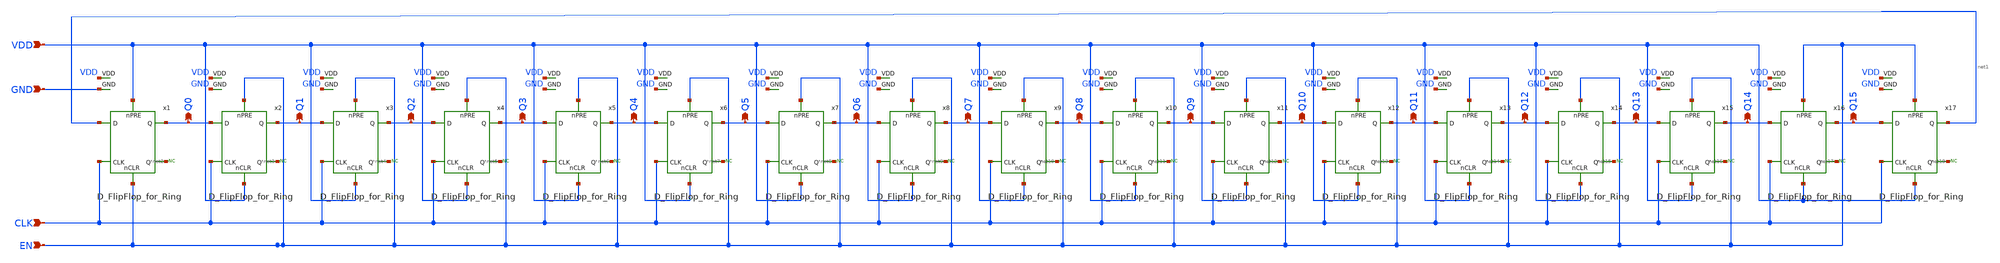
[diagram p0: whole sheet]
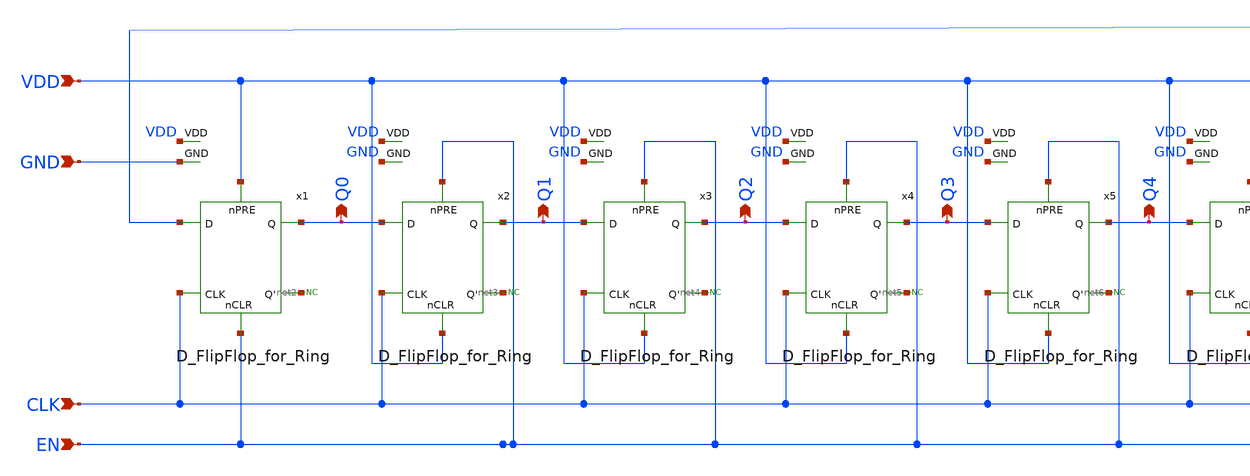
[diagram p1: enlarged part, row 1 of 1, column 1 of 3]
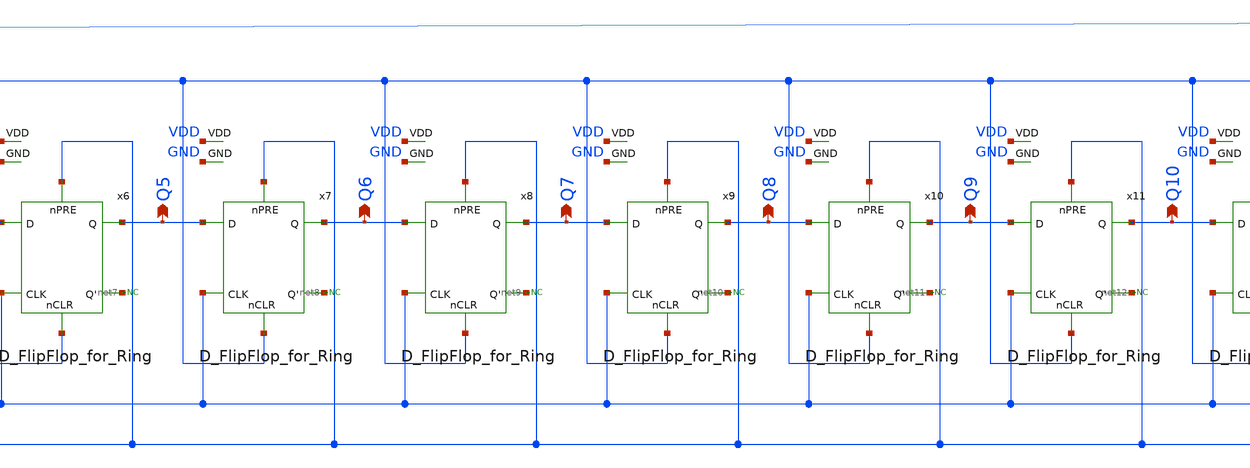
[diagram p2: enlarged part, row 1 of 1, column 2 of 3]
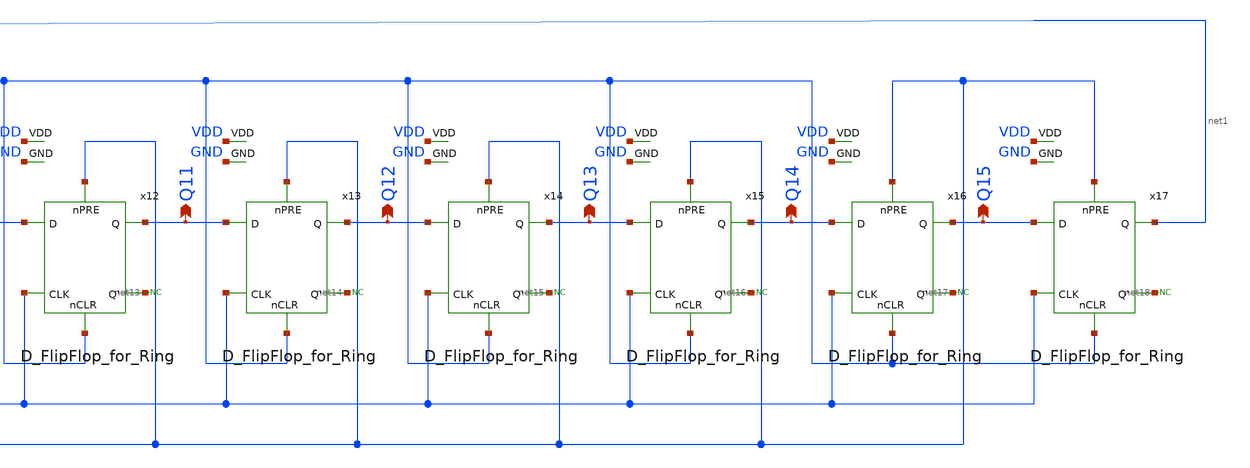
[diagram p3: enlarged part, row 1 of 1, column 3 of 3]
** sch_path: xschem/RING_COUNTER_FINAL.sch
**.subckt RING_COUNTER_FINAL Q0 Q1 Q2 Q3 Q4 Q5 Q6 Q7 Q8 Q9 Q10 Q11 Q12 Q13 Q14 Q15 CLK EN VDD GND
*.opin Q0
*.opin Q1
*.opin Q2
*.opin Q3
*.opin Q4
*.opin Q5
*.opin Q6
*.opin Q7
*.opin Q8
*.opin Q9
*.opin Q10
*.opin Q11
*.opin Q12
*.opin Q13
*.opin Q14
*.opin Q15
*.ipin CLK
*.ipin EN
*.ipin VDD
*.ipin GND
x1 VDD net1 Q0 CLK net2 EN GND VDD D_FlipFlop_for_Ring
x2 EN Q0 Q1 CLK net3 VDD GND VDD D_FlipFlop_for_Ring
x3 EN Q1 Q2 CLK net4 VDD GND VDD D_FlipFlop_for_Ring
x4 EN Q2 Q3 CLK net5 VDD GND VDD D_FlipFlop_for_Ring
x5 EN Q3 Q4 CLK net6 VDD GND VDD D_FlipFlop_for_Ring
x6 EN Q4 Q5 CLK net7 VDD GND VDD D_FlipFlop_for_Ring
x7 EN Q5 Q6 CLK net8 VDD GND VDD D_FlipFlop_for_Ring
x8 EN Q6 Q7 CLK net9 VDD GND VDD D_FlipFlop_for_Ring
x9 EN Q7 Q8 CLK net10 VDD GND VDD D_FlipFlop_for_Ring
x10 EN Q8 Q9 CLK net11 VDD GND VDD D_FlipFlop_for_Ring
x11 EN Q9 Q10 CLK net12 VDD GND VDD D_FlipFlop_for_Ring
x12 EN Q10 Q11 CLK net13 VDD GND VDD D_FlipFlop_for_Ring
x13 EN Q11 Q12 CLK net14 VDD GND VDD D_FlipFlop_for_Ring
x14 EN Q12 Q13 CLK net15 VDD GND VDD D_FlipFlop_for_Ring
x15 EN Q13 Q14 CLK net16 VDD GND VDD D_FlipFlop_for_Ring
x16 EN Q14 Q15 CLK net17 VDD GND VDD D_FlipFlop_for_Ring
x17 EN Q15 net1 CLK net18 VDD GND VDD D_FlipFlop_for_Ring
* noconn #net2
* noconn #net3
* noconn #net4
* noconn #net5
* noconn #net6
* noconn #net7
* noconn #net8
* noconn #net9
* noconn #net10
* noconn #net11
* noconn #net12
* noconn #net13
* noconn #net14
* noconn #net18
* noconn #net17
* noconn #net16
* noconn #net15
**.ends

* expanding   symbol:  D_FlipFlop_for_Ring.sym # of pins=8
** sym_path: xschem/D_FlipFlop_for_Ring.sym
** sch_path: xschem/D_FlipFlop_for_Ring.sch
.subckt D_FlipFlop_for_Ring nPRE D Q CLK Q' nCLR GND VDD
*.ipin D
*.ipin CLK
*.ipin nPRE
*.ipin nCLR
*.opin Q
*.opin Q'
*.ipin VDD
*.ipin GND
x1 net9 net10 Inverter
x2 CLK D nCLR net1 GND VDD 3-input-nand
x3 net4 net6 net7 GND VDD Nand_Gate
x4 CLK net5 nPRE net2 GND VDD 3-input-nand
x5 Q net8 nCLR Q' GND VDD 3-input-nand
x6 Q' net7 nPRE Q GND VDD 3-input-nand
x7 net3 net6 net8 GND VDD Nand_Gate
x8 net3 net1 nPRE net4 GND VDD 3-input-nand
x9 net4 net2 nCLR net3 GND VDD 3-input-nand
x10 net11 net12 Inverter
.ends


* expanding   symbol:  Inverter.sym # of pins=2
** sym_path: xschem/Standard Cells/Inverter.sym
** sch_path: xschem/Standard Cells/Inverter.sch
.subckt Inverter Vin Vout
*.opin Vout
*.ipin Vin
XM49 Vout Vin GND GND sky130_fd_pr__nfet_01v8 L=0.15 W=1 nf=1 ad='int((nf+1)/2) * W/nf * 0.29' as='int((nf+2)/2) * W/nf * 0.29'
+ pd='2*int((nf+1)/2) * (W/nf + 0.29)' ps='2*int((nf+2)/2) * (W/nf + 0.29)' nrd='0.29 / W' nrs='0.29 / W'
+ sa=0 sb=0 sd=0 mult=1 m=1
XM50 Vout Vin VDD VDD sky130_fd_pr__pfet_01v8 L=0.15 W=1 nf=1 ad='int((1 + 1)/2) * 1 / 1 * 0.29' as='int((1 + 2)/2) * 1 / 1 * 0.29'
+ pd='2*int((1 + 1)/2) * (1 / 1 + 0.29)' ps='2*int((1 + 2)/2) * (1 / 1 + 0.29)' nrd='0.29 / 1 ' nrs='0.29 / 1 '
+ sa=0 sb=0 sd=0 mult=1 m=1
.ends


* expanding   symbol:  3-input-nand.sym # of pins=6
** sym_path: xschem/3-input-nand.sym
** sch_path: xschem/3-input-nand.sch
.subckt 3-input-nand C B A Vout GND VDD
*.ipin A
*.ipin B
*.opin Vout
*.ipin C
*.ipin VDD
*.ipin GND
XM1 Vout C VDD VDD sky130_fd_pr__pfet_g5v0d10v5 L=0.720 W=1.44 nf=1 ad='int((1 + 1)/2) * 1.44 / 1 * 0.29'
+ as='int((1 + 2)/2) * 1.44 / 1 * 0.29' pd='2*int((1 + 1)/2) * (1.44 / 1 + 0.29)' ps='2*int((1 + 2)/2) * (1.44 / 1 + 0.29)'
+ nrd='0.29 / 1.44 ' nrs='0.29 / 1.44 ' sa=0 sb=0 sd=0 mult=1 m=1
XM2 Vout B VDD VDD sky130_fd_pr__pfet_g5v0d10v5 L=0.720 W=1.44 nf=1 ad='int((1 + 1)/2) * 1.44 / 1 * 0.29'
+ as='int((1 + 2)/2) * 1.44 / 1 * 0.29' pd='2*int((1 + 1)/2) * (1.44 / 1 + 0.29)' ps='2*int((1 + 2)/2) * (1.44 / 1 + 0.29)'
+ nrd='0.29 / 1.44 ' nrs='0.29 / 1.44 ' sa=0 sb=0 sd=0 mult=1 m=1
XM3 Vout A VDD VDD sky130_fd_pr__pfet_g5v0d10v5 L=0.720 W=1.44 nf=1 ad='int((1 + 1)/2) * 1.44 / 1 * 0.29'
+ as='int((1 + 2)/2) * 1.44 / 1 * 0.29' pd='2*int((1 + 1)/2) * (1.44 / 1 + 0.29)' ps='2*int((1 + 2)/2) * (1.44 / 1 + 0.29)'
+ nrd='0.29 / 1.44 ' nrs='0.29 / 1.44 ' sa=0 sb=0 sd=0 mult=1 m=1
XM4 Vout C net1 GND sky130_fd_pr__nfet_g5v0d10v5 L=1.44 W=1.44 nf=1 ad='int((1 + 1)/2) * 1.44 / 1 * 0.29'
+ as='int((1 + 2)/2) * 1.44 / 1 * 0.29' pd='2*int((1 + 1)/2) * (1.44 / 1 + 0.29)' ps='2*int((1 + 2)/2) * (1.44 / 1 + 0.29)'
+ nrd='0.29 / 1.44 ' nrs='0.29 / 1.44 ' sa=0 sb=0 sd=0 mult=1 m=1
XM5 net1 B net2 GND sky130_fd_pr__nfet_g5v0d10v5 L=1.44 W=1.44 nf=1 ad='int((1 + 1)/2) * 1.44 / 1 * 0.29'
+ as='int((1 + 2)/2) * 1.44 / 1 * 0.29' pd='2*int((1 + 1)/2) * (1.44 / 1 + 0.29)' ps='2*int((1 + 2)/2) * (1.44 / 1 + 0.29)'
+ nrd='0.29 / 1.44 ' nrs='0.29 / 1.44 ' sa=0 sb=0 sd=0 mult=1 m=1
XM6 net2 A GND GND sky130_fd_pr__nfet_g5v0d10v5 L=1.44 W=1.44 nf=1 ad='int((1 + 1)/2) * 1.44 / 1 * 0.29'
+ as='int((1 + 2)/2) * 1.44 / 1 * 0.29' pd='2*int((1 + 1)/2) * (1.44 / 1 + 0.29)' ps='2*int((1 + 2)/2) * (1.44 / 1 + 0.29)'
+ nrd='0.29 / 1.44 ' nrs='0.29 / 1.44 ' sa=0 sb=0 sd=0 mult=1 m=1
.ends


* expanding   symbol:  Nand_Gate.sym # of pins=5
** sym_path: xschem/Nand_Gate.sym
** sch_path: xschem/Nand_Gate.sch
.subckt Nand_Gate A B Vout GND VDD
*.ipin A
*.ipin B
*.ipin VDD
*.ipin GND
*.opin Vout
XM1 Vout B VDD VDD sky130_fd_pr__pfet_g5v0d10v5 L=0.720 W=1.44 nf=1 ad='int((1 + 1)/2) * 1.44 / 1 * 0.29'
+ as='int((1 + 2)/2) * 1.44 / 1 * 0.29' pd='2*int((1 + 1)/2) * (1.44 / 1 + 0.29)' ps='2*int((1 + 2)/2) * (1.44 / 1 + 0.29)'
+ nrd='0.29 / 1.44 ' nrs='0.29 / 1.44 ' sa=0 sb=0 sd=0 mult=1 m=1
XM2 Vout A VDD VDD sky130_fd_pr__pfet_g5v0d10v5 L=0.720 W=1.44 nf=1 ad='int((1 + 1)/2) * 1.44 / 1 * 0.29'
+ as='int((1 + 2)/2) * 1.44 / 1 * 0.29' pd='2*int((1 + 1)/2) * (1.44 / 1 + 0.29)' ps='2*int((1 + 2)/2) * (1.44 / 1 + 0.29)'
+ nrd='0.29 / 1.44 ' nrs='0.29 / 1.44 ' sa=0 sb=0 sd=0 mult=1 m=1
XM3 Vout B net1 GND sky130_fd_pr__nfet_g5v0d10v5 L=1.44 W=1.44 nf=1 ad='int((1 + 1)/2) * 1.44 / 1 * 0.29'
+ as='int((1 + 2)/2) * 1.44 / 1 * 0.29' pd='2*int((1 + 1)/2) * (1.44 / 1 + 0.29)' ps='2*int((1 + 2)/2) * (1.44 / 1 + 0.29)'
+ nrd='0.29 / 1.44 ' nrs='0.29 / 1.44 ' sa=0 sb=0 sd=0 mult=1 m=1
XM4 net1 A GND GND sky130_fd_pr__nfet_g5v0d10v5 L=1.44 W=1.44 nf=1 ad='int((1 + 1)/2) * 1.44 / 1 * 0.29'
+ as='int((1 + 2)/2) * 1.44 / 1 * 0.29' pd='2*int((1 + 1)/2) * (1.44 / 1 + 0.29)' ps='2*int((1 + 2)/2) * (1.44 / 1 + 0.29)'
+ nrd='0.29 / 1.44 ' nrs='0.29 / 1.44 ' sa=0 sb=0 sd=0 mult=1 m=1
.ends

.GLOBAL GND
.GLOBAL VDD
.end
